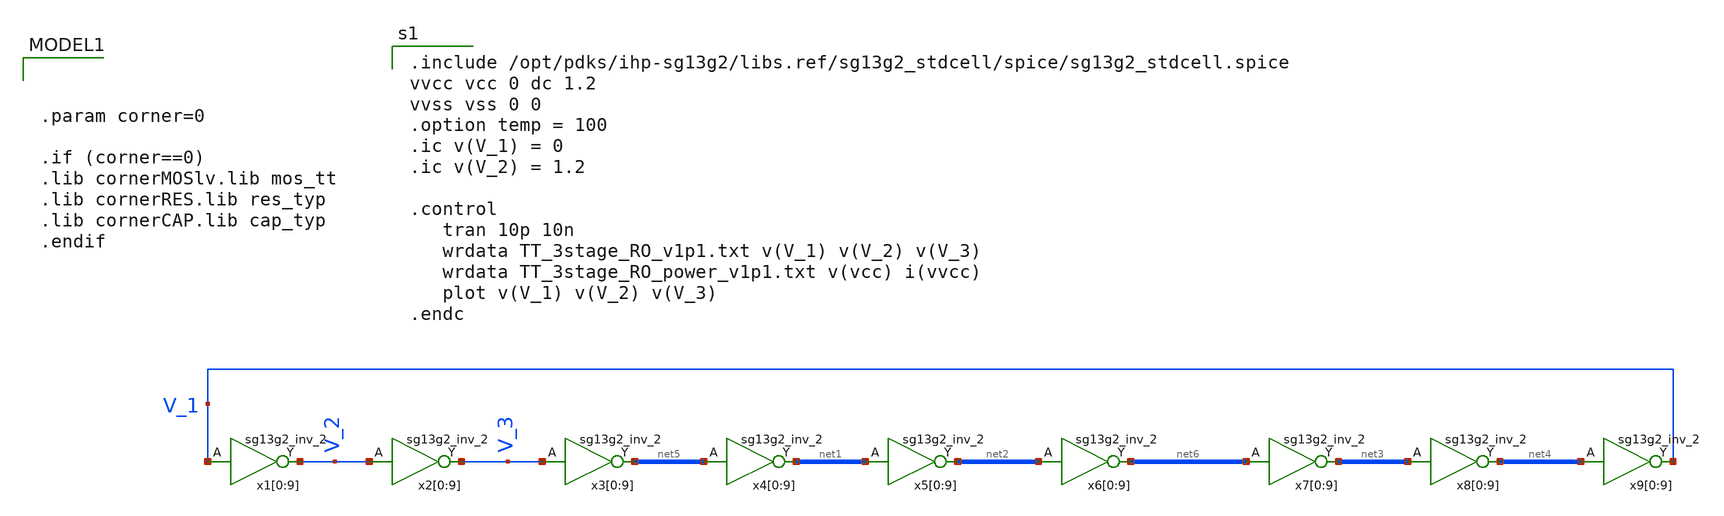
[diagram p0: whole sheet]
** sch_path: Day1/tb_9stage_RO.sch
* IHP-GmbH/IHP-Open-PDK/ihp-sg13g2/libs.tech/xschem/sg13g2_stdcells/sg13g2_inv_2.sch:
* Copyright 2023 IHP PDK Authors
* Licensed under the Apache License, Version 2.0 (the "License");
**.subckt tb_9stage_RO
x1[0] V_2 V_1 VCC VSS sg13g2_inv_2
x1[1] V_2 V_1 VCC VSS sg13g2_inv_2
x1[2] V_2 V_1 VCC VSS sg13g2_inv_2
x1[3] V_2 V_1 VCC VSS sg13g2_inv_2
x1[4] V_2 V_1 VCC VSS sg13g2_inv_2
x1[5] V_2 V_1 VCC VSS sg13g2_inv_2
x1[6] V_2 V_1 VCC VSS sg13g2_inv_2
x1[7] V_2 V_1 VCC VSS sg13g2_inv_2
x1[8] V_2 V_1 VCC VSS sg13g2_inv_2
x1[9] V_2 V_1 VCC VSS sg13g2_inv_2
x2[0] V_3 V_2 VCC VSS sg13g2_inv_2
x2[1] V_3 V_2 VCC VSS sg13g2_inv_2
x2[2] V_3 V_2 VCC VSS sg13g2_inv_2
x2[3] V_3 V_2 VCC VSS sg13g2_inv_2
x2[4] V_3 V_2 VCC VSS sg13g2_inv_2
x2[5] V_3 V_2 VCC VSS sg13g2_inv_2
x2[6] V_3 V_2 VCC VSS sg13g2_inv_2
x2[7] V_3 V_2 VCC VSS sg13g2_inv_2
x2[8] V_3 V_2 VCC VSS sg13g2_inv_2
x2[9] V_3 V_2 VCC VSS sg13g2_inv_2
x3[0] net5[9] V_3 VCC VSS sg13g2_inv_2
x3[1] net5[8] V_3 VCC VSS sg13g2_inv_2
x3[2] net5[7] V_3 VCC VSS sg13g2_inv_2
x3[3] net5[6] V_3 VCC VSS sg13g2_inv_2
x3[4] net5[5] V_3 VCC VSS sg13g2_inv_2
x3[5] net5[4] V_3 VCC VSS sg13g2_inv_2
x3[6] net5[3] V_3 VCC VSS sg13g2_inv_2
x3[7] net5[2] V_3 VCC VSS sg13g2_inv_2
x3[8] net5[1] V_3 VCC VSS sg13g2_inv_2
x3[9] net5[0] V_3 VCC VSS sg13g2_inv_2
x4[0] net1[9] net5[9] VCC VSS sg13g2_inv_2
x4[1] net1[8] net5[8] VCC VSS sg13g2_inv_2
x4[2] net1[7] net5[7] VCC VSS sg13g2_inv_2
x4[3] net1[6] net5[6] VCC VSS sg13g2_inv_2
x4[4] net1[5] net5[5] VCC VSS sg13g2_inv_2
x4[5] net1[4] net5[4] VCC VSS sg13g2_inv_2
x4[6] net1[3] net5[3] VCC VSS sg13g2_inv_2
x4[7] net1[2] net5[2] VCC VSS sg13g2_inv_2
x4[8] net1[1] net5[1] VCC VSS sg13g2_inv_2
x4[9] net1[0] net5[0] VCC VSS sg13g2_inv_2
x5[0] net2[9] net1[9] VCC VSS sg13g2_inv_2
x5[1] net2[8] net1[8] VCC VSS sg13g2_inv_2
x5[2] net2[7] net1[7] VCC VSS sg13g2_inv_2
x5[3] net2[6] net1[6] VCC VSS sg13g2_inv_2
x5[4] net2[5] net1[5] VCC VSS sg13g2_inv_2
x5[5] net2[4] net1[4] VCC VSS sg13g2_inv_2
x5[6] net2[3] net1[3] VCC VSS sg13g2_inv_2
x5[7] net2[2] net1[2] VCC VSS sg13g2_inv_2
x5[8] net2[1] net1[1] VCC VSS sg13g2_inv_2
x5[9] net2[0] net1[0] VCC VSS sg13g2_inv_2
x6[0] net6[9] net2[9] VCC VSS sg13g2_inv_2
x6[1] net6[8] net2[8] VCC VSS sg13g2_inv_2
x6[2] net6[7] net2[7] VCC VSS sg13g2_inv_2
x6[3] net6[6] net2[6] VCC VSS sg13g2_inv_2
x6[4] net6[5] net2[5] VCC VSS sg13g2_inv_2
x6[5] net6[4] net2[4] VCC VSS sg13g2_inv_2
x6[6] net6[3] net2[3] VCC VSS sg13g2_inv_2
x6[7] net6[2] net2[2] VCC VSS sg13g2_inv_2
x6[8] net6[1] net2[1] VCC VSS sg13g2_inv_2
x6[9] net6[0] net2[0] VCC VSS sg13g2_inv_2
x7[0] net3[9] net6[9] VCC VSS sg13g2_inv_2
x7[1] net3[8] net6[8] VCC VSS sg13g2_inv_2
x7[2] net3[7] net6[7] VCC VSS sg13g2_inv_2
x7[3] net3[6] net6[6] VCC VSS sg13g2_inv_2
x7[4] net3[5] net6[5] VCC VSS sg13g2_inv_2
x7[5] net3[4] net6[4] VCC VSS sg13g2_inv_2
x7[6] net3[3] net6[3] VCC VSS sg13g2_inv_2
x7[7] net3[2] net6[2] VCC VSS sg13g2_inv_2
x7[8] net3[1] net6[1] VCC VSS sg13g2_inv_2
x7[9] net3[0] net6[0] VCC VSS sg13g2_inv_2
x8[0] net4[9] net3[9] VCC VSS sg13g2_inv_2
x8[1] net4[8] net3[8] VCC VSS sg13g2_inv_2
x8[2] net4[7] net3[7] VCC VSS sg13g2_inv_2
x8[3] net4[6] net3[6] VCC VSS sg13g2_inv_2
x8[4] net4[5] net3[5] VCC VSS sg13g2_inv_2
x8[5] net4[4] net3[4] VCC VSS sg13g2_inv_2
x8[6] net4[3] net3[3] VCC VSS sg13g2_inv_2
x8[7] net4[2] net3[2] VCC VSS sg13g2_inv_2
x8[8] net4[1] net3[1] VCC VSS sg13g2_inv_2
x8[9] net4[0] net3[0] VCC VSS sg13g2_inv_2
x9[0] V_1 net4[9] VCC VSS sg13g2_inv_2
x9[1] V_1 net4[8] VCC VSS sg13g2_inv_2
x9[2] V_1 net4[7] VCC VSS sg13g2_inv_2
x9[3] V_1 net4[6] VCC VSS sg13g2_inv_2
x9[4] V_1 net4[5] VCC VSS sg13g2_inv_2
x9[5] V_1 net4[4] VCC VSS sg13g2_inv_2
x9[6] V_1 net4[3] VCC VSS sg13g2_inv_2
x9[7] V_1 net4[2] VCC VSS sg13g2_inv_2
x9[8] V_1 net4[1] VCC VSS sg13g2_inv_2
x9[9] V_1 net4[0] VCC VSS sg13g2_inv_2
**** begin user architecture code

.include /opt/pdks/ihp-sg13g2/libs.ref/sg13g2_stdcell/spice/sg13g2_stdcell.spice
vvcc vcc 0 dc 1.2
vvss vss 0 0
.option temp = 100
.ic v(V_1) = 0
.ic v(V_2) = 1.2

.control
   tran 10p 10n
   wrdata TT_3stage_RO_v1p1.txt v(V_1) v(V_2) v(V_3)
   wrdata TT_3stage_RO_power_v1p1.txt v(vcc) i(vvcc)
   plot v(V_1) v(V_2) v(V_3)
.endc




.param corner=0

.if (corner==0)
.lib cornerMOSlv.lib mos_tt
.lib cornerRES.lib res_typ
.lib cornerCAP.lib cap_typ
.endif

**** end user architecture code
**.ends

* expanding   symbol:  sg13g2_inv_2.sym # of pins=2
** sym_path: sg13g2_inv_2.sym
** sch_path: sg13g2_inv_2.sch
.subckt sg13g2_inv_2 Y A VDD VSS
*.opin Y
*.ipin A
*.iopin VDD
*.iopin VSS
XM1 Y A VSS VSS sg13_lv_nmos w=1.48u l=130.00n ng=2 m=1 mm_ok=1
XM2 Y A VDD VDD sg13_lv_pmos w=2.24u l=130.00n ng=2 m=1 mm_ok=1
.ends

.end
